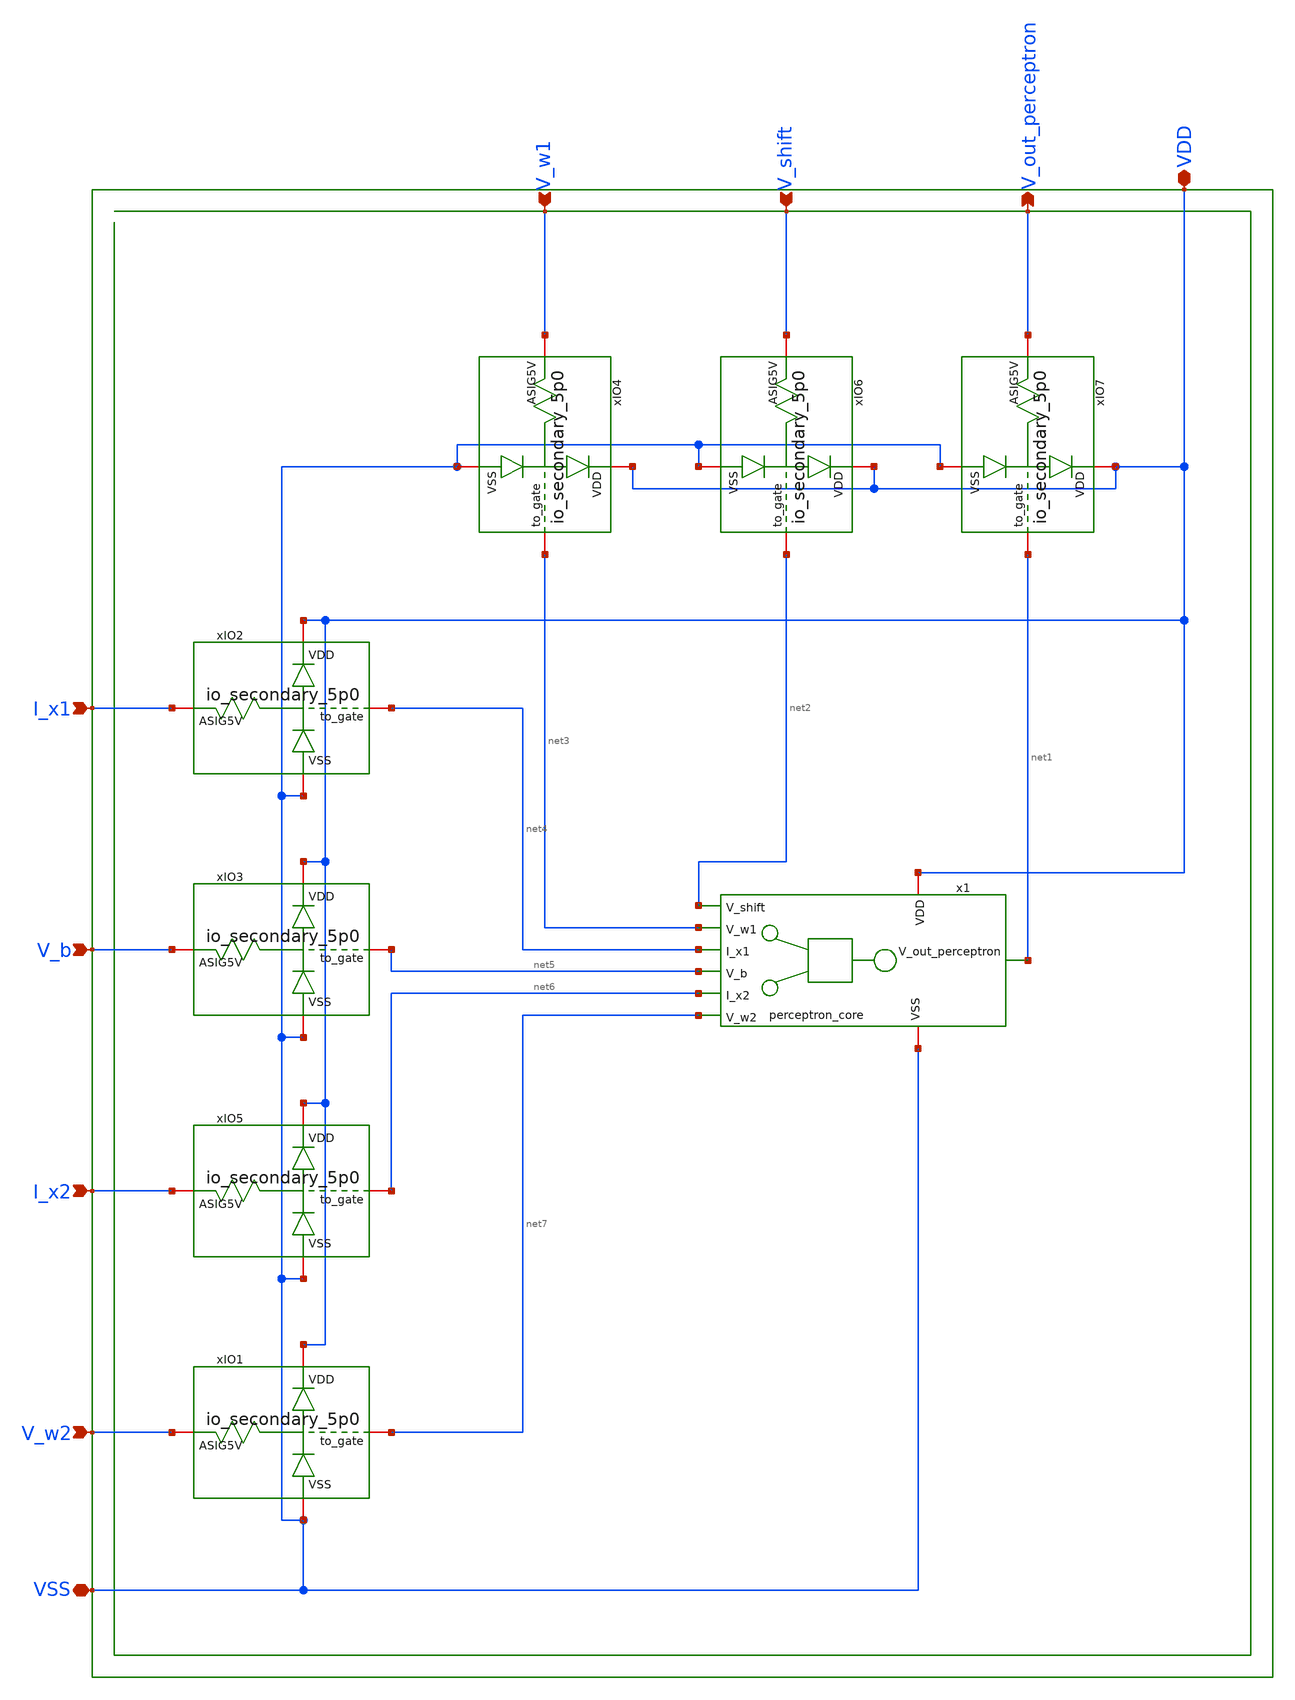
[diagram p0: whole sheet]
** sch_path: lvs/schematics/perceptron.sch
**.subckt perceptron VDD VSS I_x1 I_x2 V_b V_w2 V_w1 V_shift V_out_perceptron
*.iopin VDD
*.iopin VSS
*.ipin I_x1
*.ipin I_x2
*.ipin V_b
*.ipin V_w2
*.ipin V_w1
*.ipin V_shift
*.opin V_out_perceptron
x1 VDD net2 net3 net4 net1 net5 net6 net7 VSS perceptron_core
XxIO5 VDD net6 I_x2 VSS io_secondary_5p0
XxIO1 VDD net7 V_w2 VSS io_secondary_5p0
XxIO2 VDD net4 I_x1 VSS io_secondary_5p0
XxIO3 VDD net5 V_b VSS io_secondary_5p0
XxIO4 VDD net3 V_w1 VSS io_secondary_5p0
XxIO6 VDD net2 V_shift VSS io_secondary_5p0
XxIO7 VDD net1 V_out_perceptron VSS io_secondary_5p0
**.ends
.end
